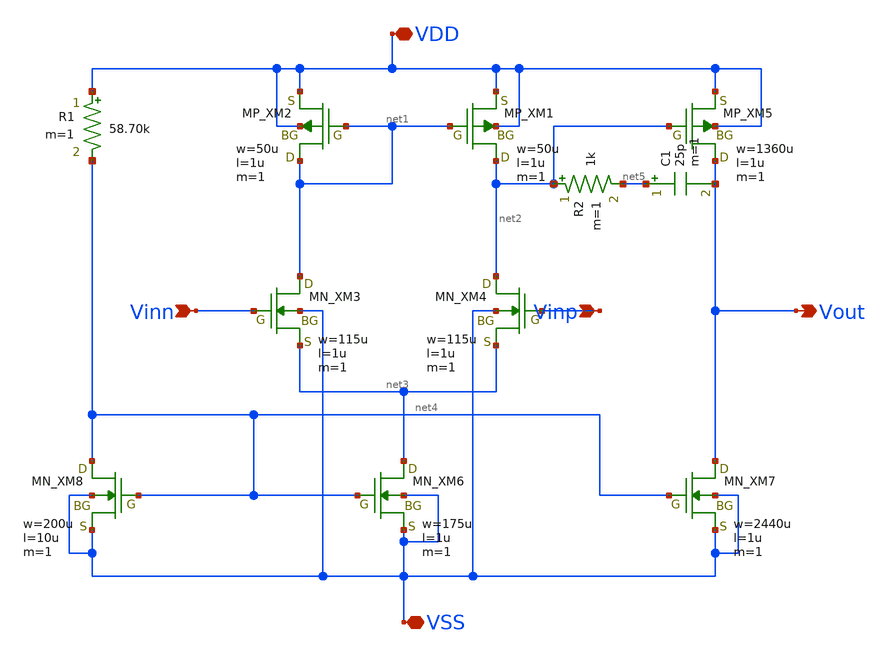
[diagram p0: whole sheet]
** sch_path: OPAF2026/opamp2.sch
**.subckt opamp2 Vout VDD VSS Vinn Vinp
*.opin Vout
*.iopin VDD
*.iopin VSS
*.ipin Vinn
*.ipin Vinp
XXM1 net2 net1 VDD VDD PMOS w=50u l=1u nrd=0 nrs=0 m=1
XXM2 net1 net1 VDD VDD PMOS w=50u l=1u nrd=0 nrs=0 m=1
XXM3 net1 Vinn net3 VSS NMOS w=115u l=1u nrd=0 nrs=0 m=1
XXM4 net2 Vinp net3 VSS NMOS w=115u l=1u nrd=0 nrs=0 m=1
XXM5 Vout net2 VDD VDD PMOS w=1360u l=1u nrd=0 nrs=0 m=1
XXM6 net3 net4 VSS VSS NMOS w=175u l=1u nrd=0 nrs=0 m=1
XXM7 Vout net4 VSS VSS NMOS w=2440u l=1u nrd=0 nrs=0 m=1
XXM8 net4 net4 VSS VSS NMOS w=200u l=10u nrd=0 nrs=0 m=1
C1 net5 Vout 25p m=1
R1 VDD net4 58.70k m=1
R2 net2 net5 1k m=1
**.ends
.end
